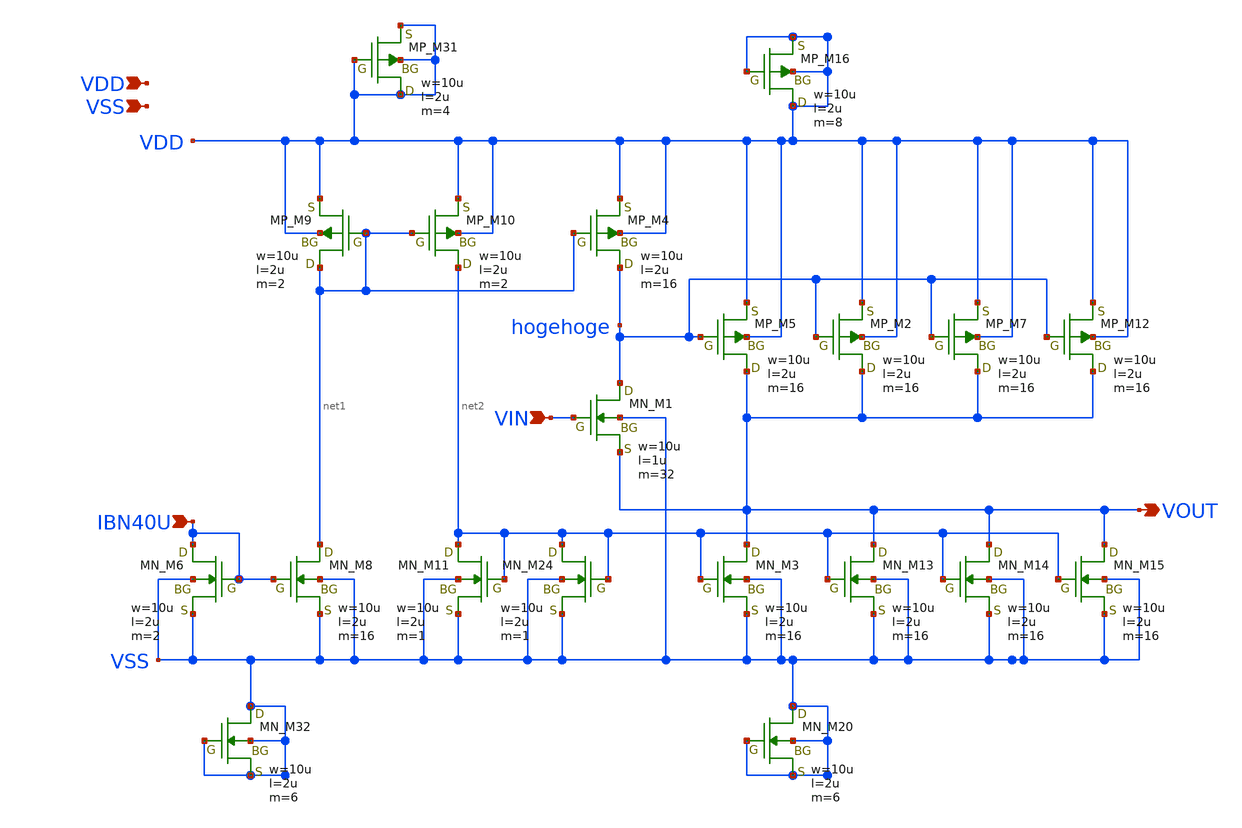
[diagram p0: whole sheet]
** sch_path: member_project/JJY_Receiver/Masahiro/jjy_recv/OBUF_SSF/OBUF_SSF.sch
**.subckt OBUF_SSF VDD VSS VIN IBN40U VOUT
*.ipin VDD
*.ipin VSS
*.ipin VIN
*.ipin IBN40U
*.opin VOUT
XM1 hogehoge VIN VOUT VSS NMOS w=10u l=1u as=0 ad=0 ps=0 pd=0 nrd=0 nrs=0 m=32
XM3 VOUT net2 VSS VSS NMOS w=10u l=2u as=0 ad=0 ps=0 pd=0 nrd=0 nrs=0 m=16
XM6 IBN40U IBN40U VSS VSS NMOS w=10u l=2u as=0 ad=0 ps=0 pd=0 nrd=0 nrs=0 m=2
XM4 hogehoge net1 VDD VDD PMOS w=10u l=2u as=0 ad=0 ps=0 pd=0 nrd=0 nrs=0 m=16
XM5 VOUT hogehoge VDD VDD PMOS w=10u l=2u as=0 ad=0 ps=0 pd=0 nrd=0 nrs=0 m=16
XM8 net1 IBN40U VSS VSS NMOS w=10u l=2u as=0 ad=0 ps=0 pd=0 nrd=0 nrs=0 m=16
XM9 net1 net1 VDD VDD PMOS w=10u l=2u as=0 ad=0 ps=0 pd=0 nrd=0 nrs=0 m=2
XM10 net2 net1 VDD VDD PMOS w=10u l=2u as=0 ad=0 ps=0 pd=0 nrd=0 nrs=0 m=2
XM11 net2 net2 VSS VSS NMOS w=10u l=2u as=0 ad=0 ps=0 pd=0 nrd=0 nrs=0 m=1
XM2 VOUT hogehoge VDD VDD PMOS w=10u l=2u as=0 ad=0 ps=0 pd=0 nrd=0 nrs=0 m=16
XM7 VOUT hogehoge VDD VDD PMOS w=10u l=2u as=0 ad=0 ps=0 pd=0 nrd=0 nrs=0 m=16
XM12 VOUT hogehoge VDD VDD PMOS w=10u l=2u as=0 ad=0 ps=0 pd=0 nrd=0 nrs=0 m=16
XM13 VOUT net2 VSS VSS NMOS w=10u l=2u as=0 ad=0 ps=0 pd=0 nrd=0 nrs=0 m=16
XM14 VOUT net2 VSS VSS NMOS w=10u l=2u as=0 ad=0 ps=0 pd=0 nrd=0 nrs=0 m=16
XM15 VOUT net2 VSS VSS NMOS w=10u l=2u as=0 ad=0 ps=0 pd=0 nrd=0 nrs=0 m=16
XM16 VDD VDD VDD VDD PMOS w=10u l=2u as=0 ad=0 ps=0 pd=0 nrd=0 nrs=0 m=8
XM24 net2 net2 VSS VSS NMOS w=10u l=2u as=0 ad=0 ps=0 pd=0 nrd=0 nrs=0 m=1
XM20 VSS VSS VSS VSS NMOS w=10u l=2u as=0 ad=0 ps=0 pd=0 nrd=0 nrs=0 m=6
XM31 VDD VDD VDD VDD PMOS w=10u l=2u as=0 ad=0 ps=0 pd=0 nrd=0 nrs=0 m=4
XM32 VSS VSS VSS VSS NMOS w=10u l=2u as=0 ad=0 ps=0 pd=0 nrd=0 nrs=0 m=6
**.ends
.end
